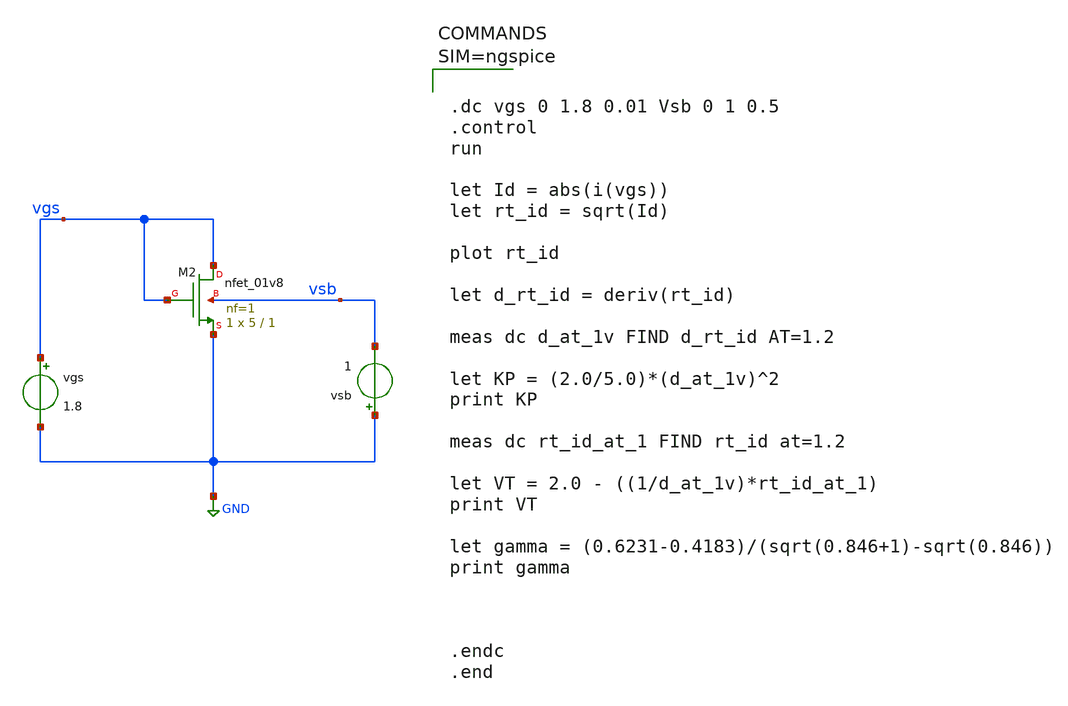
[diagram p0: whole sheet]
** sch_path: xschem/param_nw.sch
**.subckt param_nw
vsb GND vsb 1
vgs vgs GND 1.8
XM2 vgs vgs GND vsb sky130_fd_pr__nfet_01v8 L=1 W=5 nf=1 ad='int((1 + 1)/2) * 5 / 1 * 0.29' as='int((1 + 2)/2) * 5 / 1 * 0.29'
+ pd='2*int((1 + 1)/2) * (5 / 1 + 0.29)' ps='2*int((1 + 2)/2) * (5 / 1 + 0.29)' nrd='0.29 / 5 ' nrs='0.29 / 5 '
+ sa=0 sb=0 sd=0 mult=1 m=1
**** begin user architecture code

** opencircuitdesign pdks install
.lib $::SKYWATER_MODELS/sky130.lib.spice tt




.dc vgs 0 1.8 0.01 Vsb 0 1 0.5
.control
run

let Id = abs(i(vgs))
let rt_id = sqrt(Id)

plot rt_id

let d_rt_id = deriv(rt_id)

meas dc d_at_1v FIND d_rt_id AT=1.2

let KP = (2.0/5.0)*(d_at_1v)^2
print KP

meas dc rt_id_at_1 FIND rt_id at=1.2

let VT = 2.0 - ((1/d_at_1v)*rt_id_at_1)
print VT

let gamma = (0.6231-0.4183)/(sqrt(0.846+1)-sqrt(0.846))
print gamma



.endc
.end



**** end user architecture code
**.ends
.GLOBAL GND
.end
